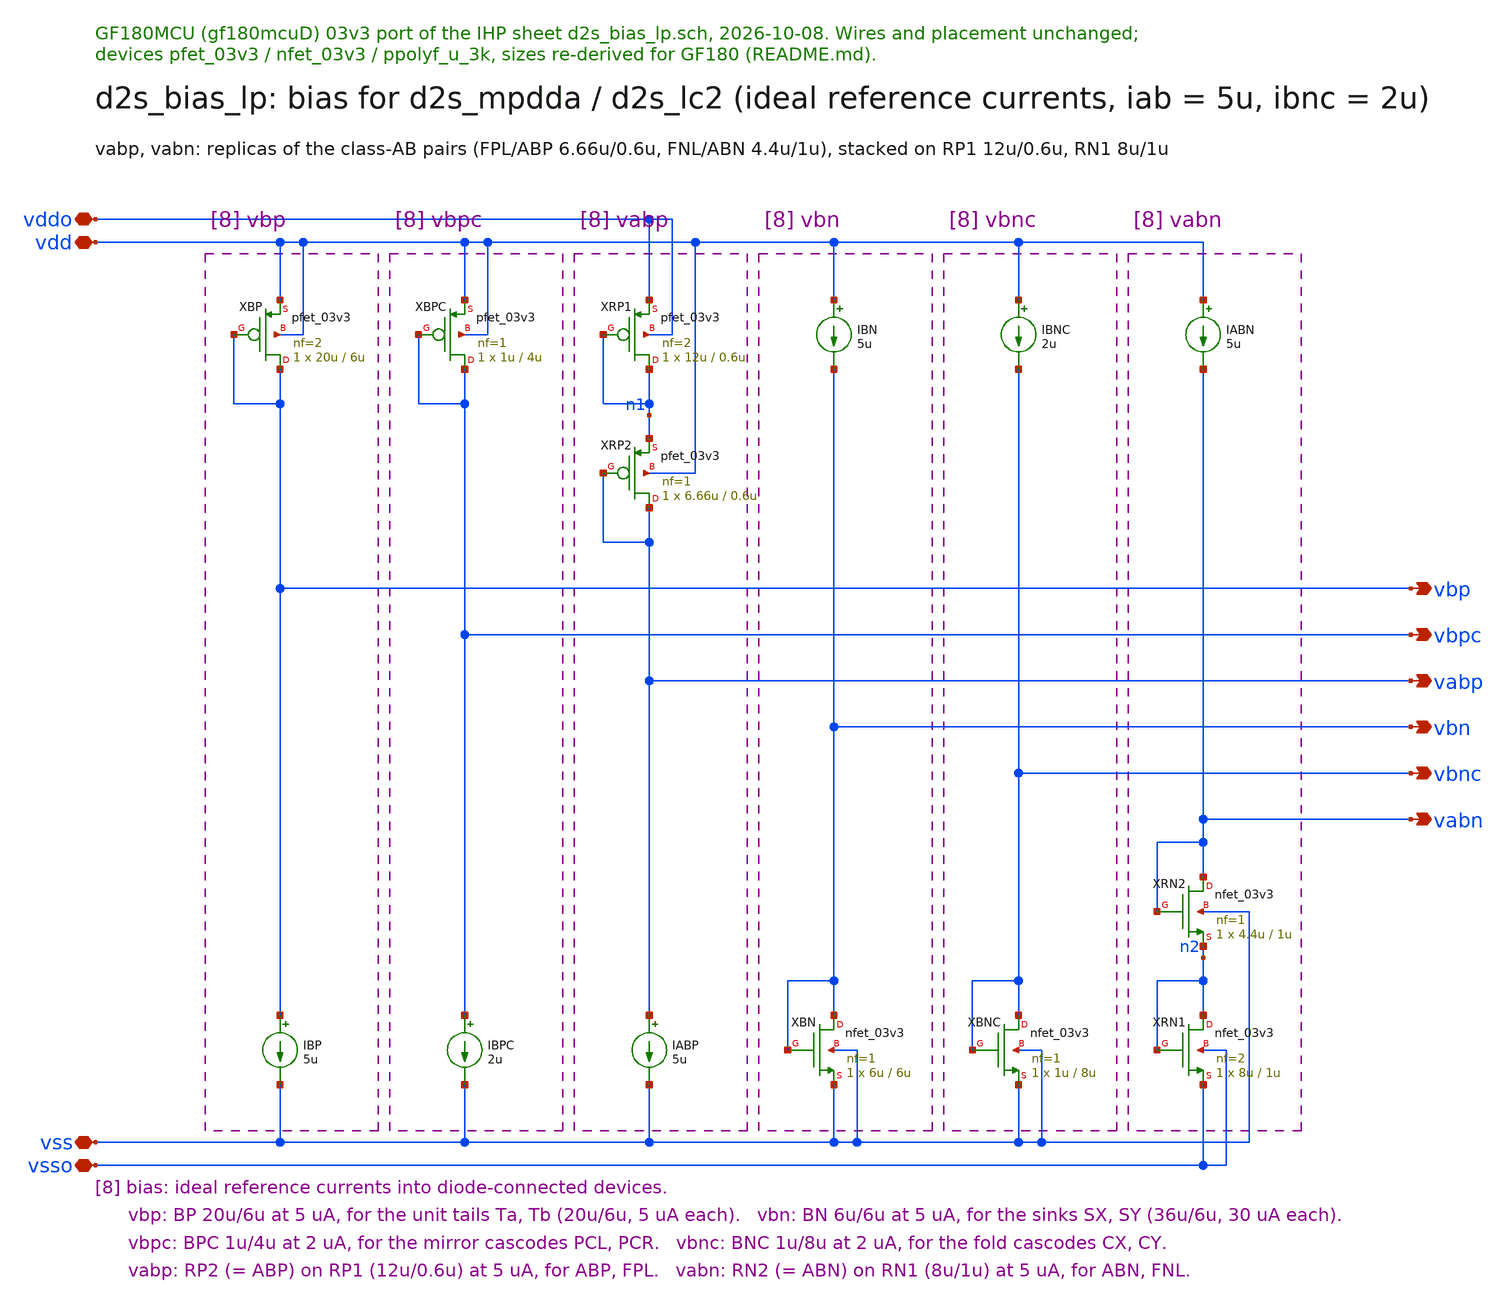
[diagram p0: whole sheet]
** sch_path: macros/ClassABBias/schematic/xschem/ClassABBiasIdeal.sch
**.subckt ClassABBiasIdeal vdd vss vddo vsso vbp vbn vbpc vbnc vabp vabn
*.iopin vdd
*.iopin vss
*.iopin vddo
*.iopin vsso
*.opin vbp
*.opin vbn
*.opin vbpc
*.opin vbnc
*.opin vabp
*.opin vabn
XBP vbp vbp vdd vdd pfet_03v3 L=6u W=20u nf=2 ad='int((nf+1)/2) * W/nf * 0.18u' as='int((nf+2)/2) * W/nf * 0.18u'
+ pd='2*int((nf+1)/2) * (W/nf + 0.18u)' ps='2*int((nf+2)/2) * (W/nf + 0.18u)' nrd='0.18u / W' nrs='0.18u / W'
+ sa=0 sb=0 sd=0 m=1
IBP vbp vss 5u
XBPC vbpc vbpc vdd vdd pfet_03v3 L=4u W=1u nf=1 ad='int((nf+1)/2) * W/nf * 0.18u' as='int((nf+2)/2) * W/nf * 0.18u'
+ pd='2*int((nf+1)/2) * (W/nf + 0.18u)' ps='2*int((nf+2)/2) * (W/nf + 0.18u)' nrd='0.18u / W' nrs='0.18u / W'
+ sa=0 sb=0 sd=0 m=1
IBPC vbpc vss 2u
XRP1 n1 n1 vddo vddo pfet_03v3 L=0.6u W=12u nf=2 ad='int((nf+1)/2) * W/nf * 0.18u' as='int((nf+2)/2) * W/nf * 0.18u'
+ pd='2*int((nf+1)/2) * (W/nf + 0.18u)' ps='2*int((nf+2)/2) * (W/nf + 0.18u)' nrd='0.18u / W' nrs='0.18u / W'
+ sa=0 sb=0 sd=0 m=1
XRP2 vabp vabp n1 vdd pfet_03v3 L=0.6u W=6.66u nf=1 ad='int((nf+1)/2) * W/nf * 0.18u' as='int((nf+2)/2) * W/nf * 0.18u'
+ pd='2*int((nf+1)/2) * (W/nf + 0.18u)' ps='2*int((nf+2)/2) * (W/nf + 0.18u)' nrd='0.18u / W' nrs='0.18u / W'
+ sa=0 sb=0 sd=0 m=1
IABP vabp vss 5u
IBN vdd vbn 5u
XBN vbn vbn vss vss nfet_03v3 L=6u W=6u nf=1 ad='int((nf+1)/2) * W/nf * 0.18u' as='int((nf+2)/2) * W/nf * 0.18u'
+ pd='2*int((nf+1)/2) * (W/nf + 0.18u)' ps='2*int((nf+2)/2) * (W/nf + 0.18u)' nrd='0.18u / W' nrs='0.18u / W'
+ sa=0 sb=0 sd=0 m=1
IBNC vdd vbnc 2u
XBNC vbnc vbnc vss vss nfet_03v3 L=8u W=1u nf=1 ad='int((nf+1)/2) * W/nf * 0.18u' as='int((nf+2)/2) * W/nf * 0.18u'
+ pd='2*int((nf+1)/2) * (W/nf + 0.18u)' ps='2*int((nf+2)/2) * (W/nf + 0.18u)' nrd='0.18u / W' nrs='0.18u / W'
+ sa=0 sb=0 sd=0 m=1
IABN vdd vabn 5u
XRN2 vabn vabn n2 vss nfet_03v3 L=1u W=4.4u nf=1 ad='int((nf+1)/2) * W/nf * 0.18u' as='int((nf+2)/2) * W/nf * 0.18u'
+ pd='2*int((nf+1)/2) * (W/nf + 0.18u)' ps='2*int((nf+2)/2) * (W/nf + 0.18u)' nrd='0.18u / W' nrs='0.18u / W'
+ sa=0 sb=0 sd=0 m=1
XRN1 n2 n2 vsso vsso nfet_03v3 L=1u W=8u nf=2 ad='int((nf+1)/2) * W/nf * 0.18u' as='int((nf+2)/2) * W/nf * 0.18u'
+ pd='2*int((nf+1)/2) * (W/nf + 0.18u)' ps='2*int((nf+2)/2) * (W/nf + 0.18u)' nrd='0.18u / W' nrs='0.18u / W'
+ sa=0 sb=0 sd=0 m=1
**.ends
.end
